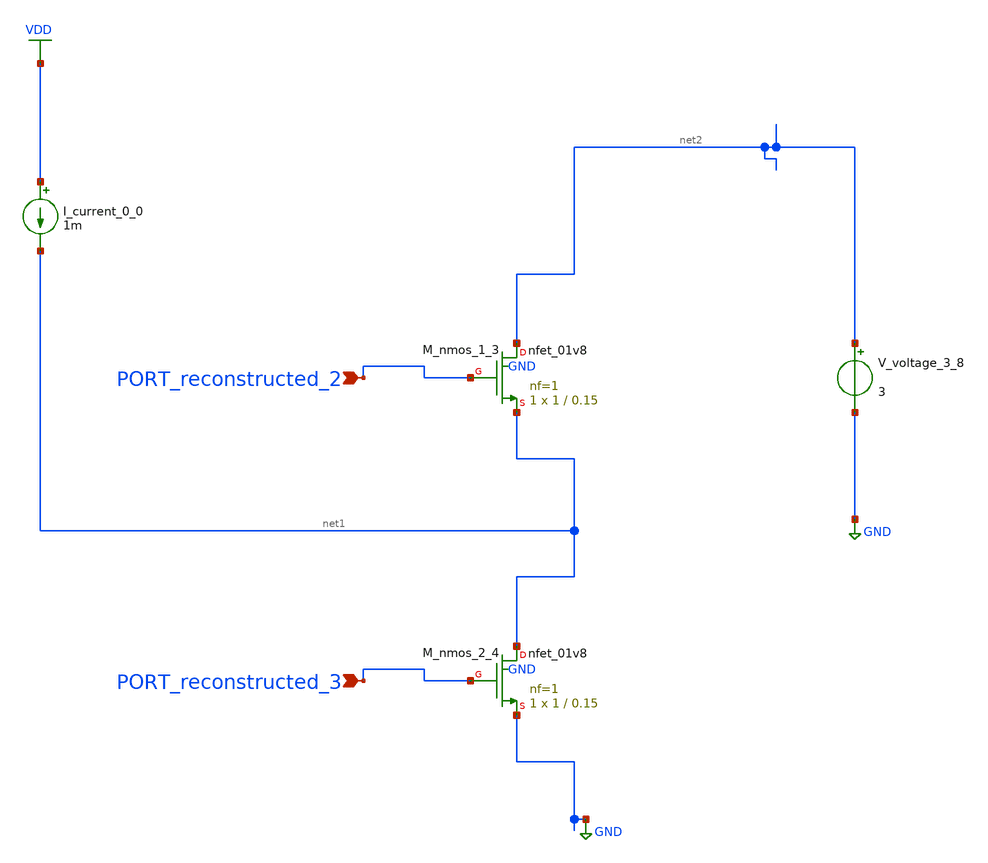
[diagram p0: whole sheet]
** sch_path: schematics/AMSNet/164.sch
**.subckt 164 PORT_reconstructed_2 PORT_reconstructed_3
*.ipin PORT_reconstructed_2
*.ipin PORT_reconstructed_3
I_current_0_0 VDD net1 1m
XM_nmos_1_3 net2 PORT_reconstructed_2 net1 GND sky130_fd_pr__nfet_01v8 L=0.15 W=1 nf=1 ad='int((1 + 1)/2) * 1 / 1 * 0.29'
+ as='int((1 + 2)/2) * 1 / 1 * 0.29' pd='2*int((1 + 1)/2) * (1 / 1 + 0.29)' ps='2*int((1 + 2)/2) * (1 / 1 + 0.29)'
+ nrd='0.29 / 1 ' nrs='0.29 / 1 ' sa=0 sb=0 sd=0 mult=1 m=1
XM_nmos_2_4 net1 PORT_reconstructed_3 GND GND sky130_fd_pr__nfet_01v8 L=0.15 W=1 nf=1 ad='int((1 + 1)/2) * 1 / 1 * 0.29'
+ as='int((1 + 2)/2) * 1 / 1 * 0.29' pd='2*int((1 + 1)/2) * (1 / 1 + 0.29)' ps='2*int((1 + 2)/2) * (1 / 1 + 0.29)'
+ nrd='0.29 / 1 ' nrs='0.29 / 1 ' sa=0 sb=0 sd=0 mult=1 m=1
V_voltage_3_8 net2 GND 3
**.ends
.GLOBAL GND
.GLOBAL VDD
.end
